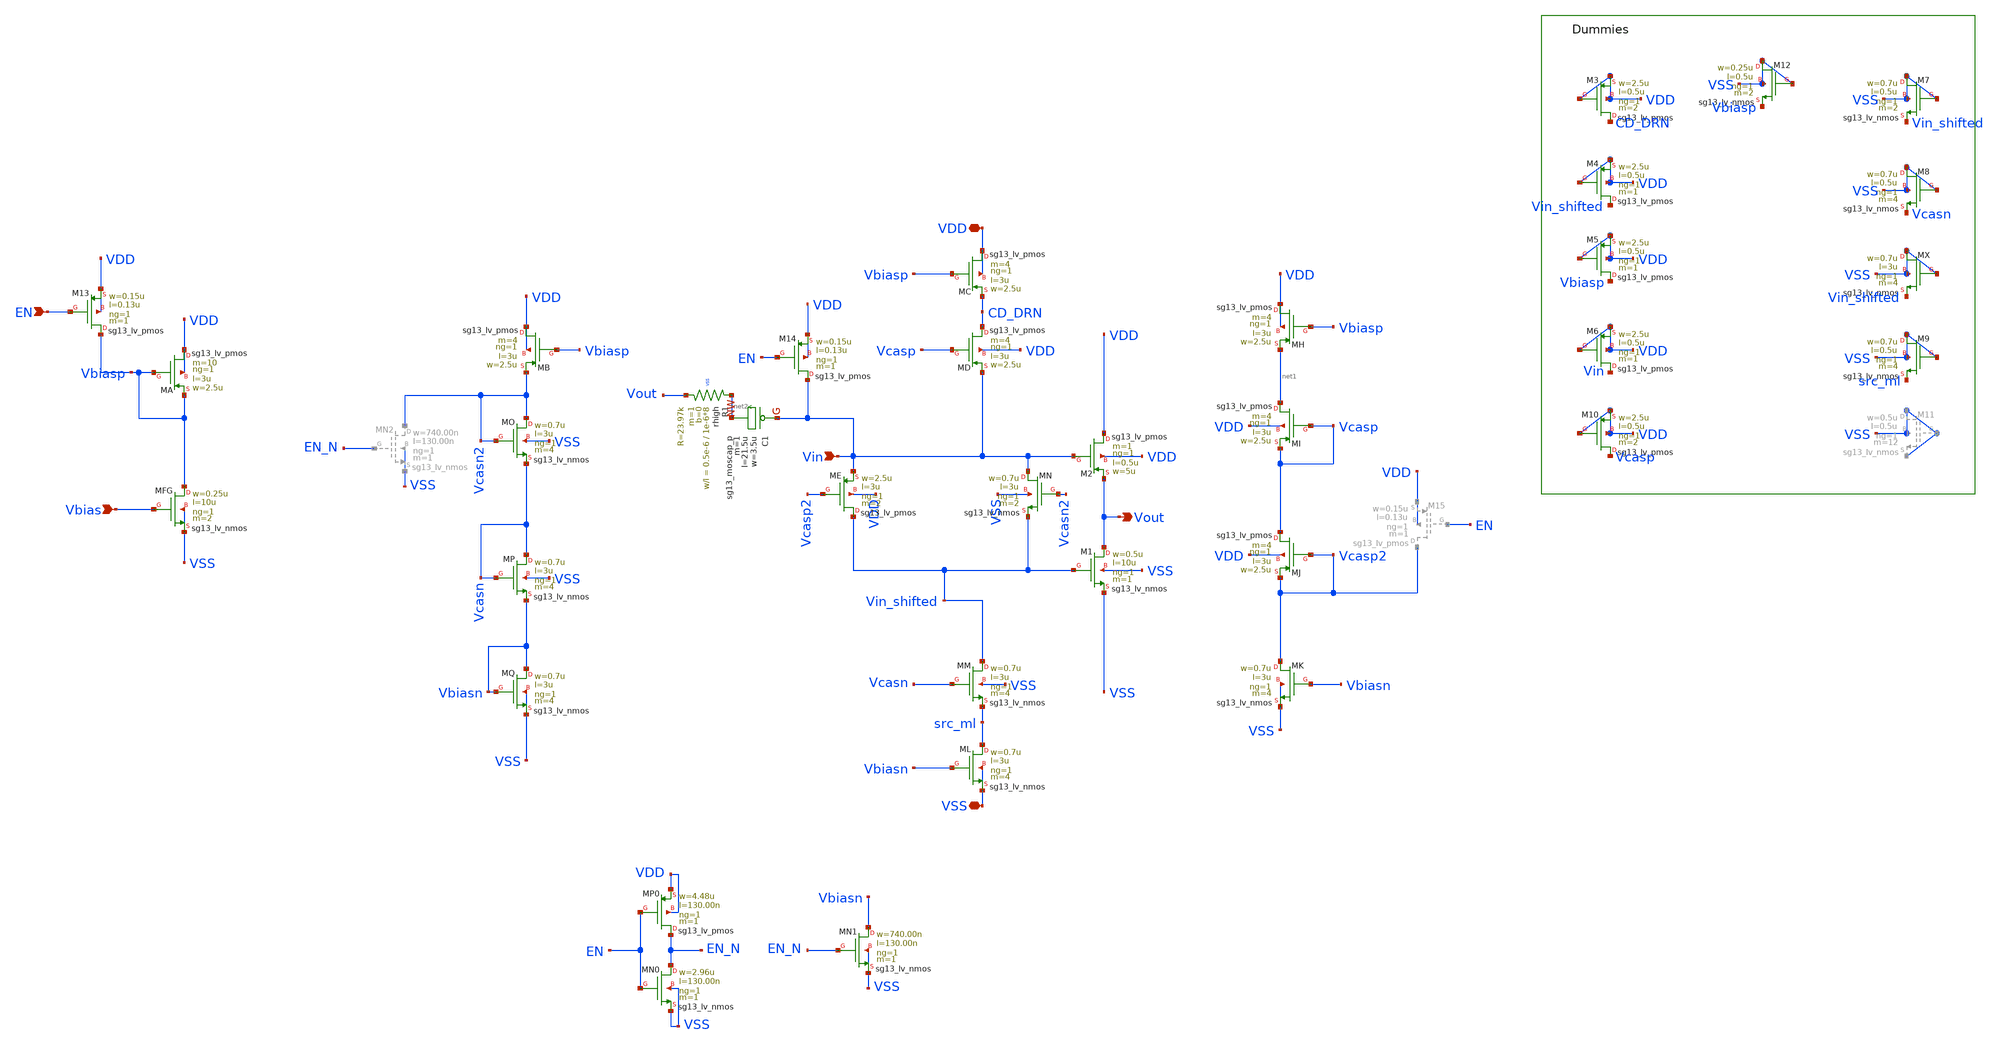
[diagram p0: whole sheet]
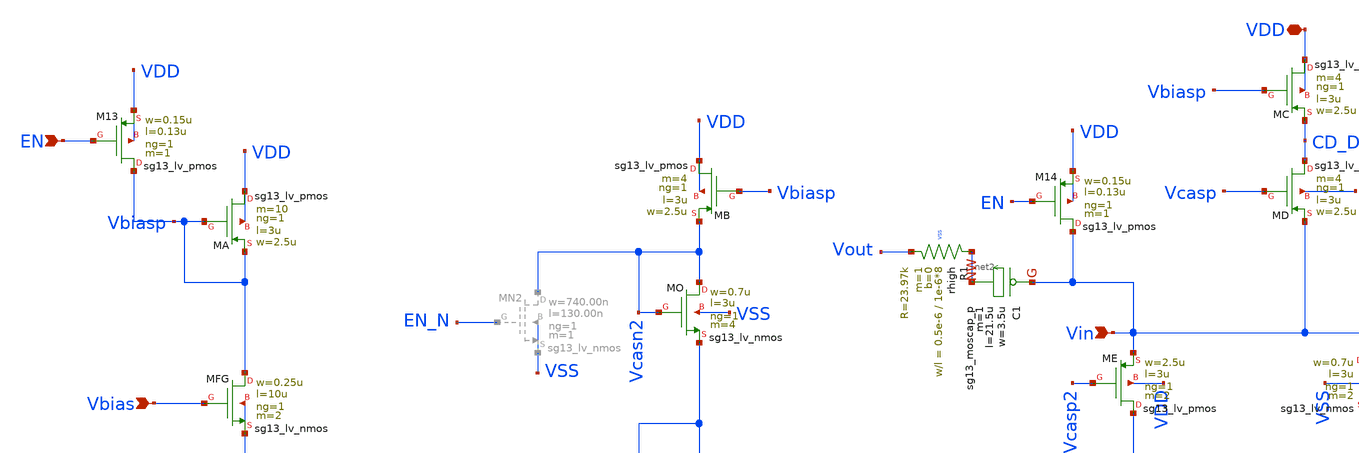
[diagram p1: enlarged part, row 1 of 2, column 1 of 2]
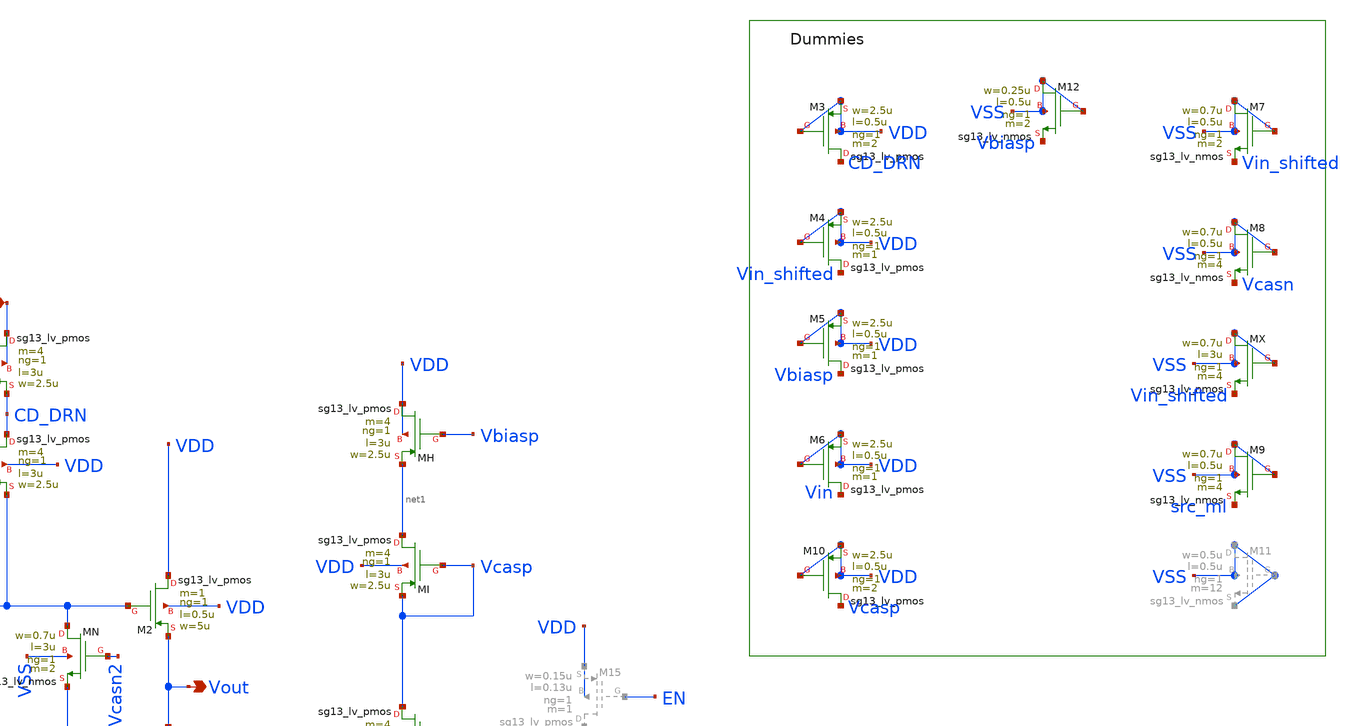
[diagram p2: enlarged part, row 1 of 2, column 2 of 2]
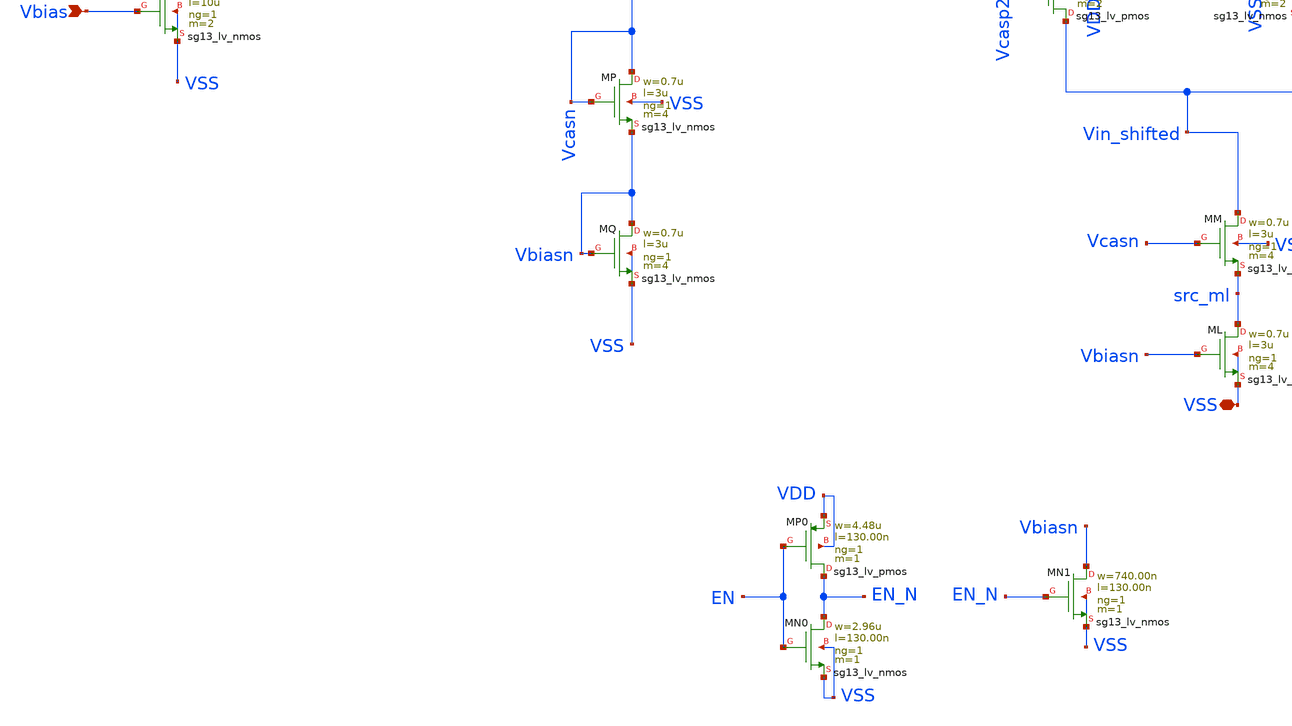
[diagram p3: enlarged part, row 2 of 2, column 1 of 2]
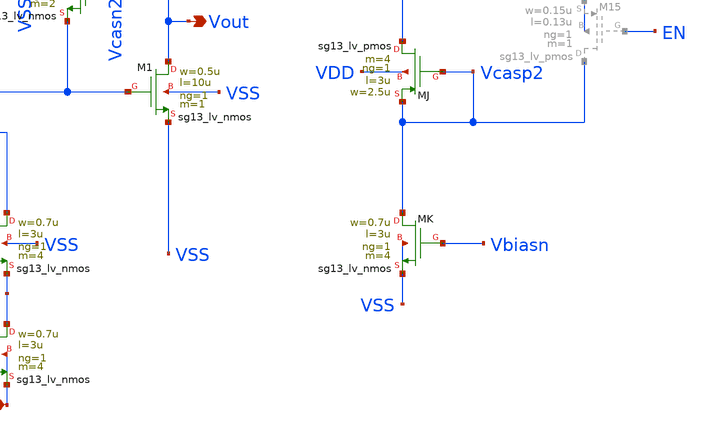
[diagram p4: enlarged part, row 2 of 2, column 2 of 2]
** sch_path: schema/ota_cmfb_core/ota_cmfb_core_push_pull_output_stage.sch
**.subckt ota_cmfb_core_push_pull_output_stage VSS VDD Vbias Vin Vout EN
*.iopin VSS
*.iopin VDD
*.ipin Vbias
*.ipin Vin
*.opin Vout
*.ipin EN
XM1 Vout Vin_shifted VSS VSS sg13_lv_nmos w=0.5u l=10u ng=1 m=1 mm_ok=1
XM2 VDD Vin Vout VDD sg13_lv_pmos w=5u l=0.5u ng=1 m=1 mm_ok=1
XMC VDD Vbiasp CD_DRN VDD sg13_lv_pmos w=2.5u l=3u ng=1 m=4 mm_ok=1
XME Vin_shifted Vcasp2 Vin VDD sg13_lv_pmos w=2.5u l=3u ng=1 m=2 mm_ok=1
XMD CD_DRN Vcasp Vin VDD sg13_lv_pmos w=2.5u l=3u ng=1 m=4 mm_ok=1
XMN Vin Vcasn2 Vin_shifted VSS sg13_lv_nmos w=0.7u l=3u ng=1 m=2 mm_ok=1
XMH VDD Vbiasp net1 VDD sg13_lv_pmos w=2.5u l=3u ng=1 m=4 mm_ok=1
XMI net1 Vcasp Vcasp VDD sg13_lv_pmos w=2.5u l=3u ng=1 m=4 mm_ok=1
XMJ Vcasp Vcasp2 Vcasp2 VDD sg13_lv_pmos w=2.5u l=3u ng=1 m=4 mm_ok=1
XMB VDD Vbiasp Vcasn2 VDD sg13_lv_pmos w=2.5u l=3u ng=1 m=4 mm_ok=1
XMO Vcasn2 Vcasn2 Vcasn VSS sg13_lv_nmos w=0.7u l=3u ng=1 m=4 mm_ok=1
XR1 net2 Vout VSS rhigh w=0.5e-6 l=1e-6*8 m=1 b=0 mm_ok=1
XC1 Vin net2 sg13_moscap_p w=3.5u l=21.5u m=1 mm_ok=1
XMFG Vbiasp Vbias VSS VSS sg13_lv_nmos w=0.25u l=10u ng=1 m=2 mm_ok=1
XMA VDD Vbiasp Vbiasp VDD sg13_lv_pmos w=2.5u l=3u ng=1 m=10 mm_ok=1
XMP Vcasn Vcasn Vbiasn VSS sg13_lv_nmos w=0.7u l=3u ng=1 m=4 mm_ok=1
XMQ Vbiasn Vbiasn VSS VSS sg13_lv_nmos w=0.7u l=3u ng=1 m=4 mm_ok=1
XMM Vin_shifted Vcasn src_ml VSS sg13_lv_nmos w=0.7u l=3u ng=1 m=4 mm_ok=1
XML src_ml Vbiasn VSS VSS sg13_lv_nmos w=0.7u l=3u ng=1 m=4 mm_ok=1
XMK Vcasp2 Vbiasn VSS VSS sg13_lv_nmos w=0.7u l=3u ng=1 m=4 mm_ok=1
XM3 CD_DRN VDD VDD VDD sg13_lv_pmos w=2.5u l=0.5u ng=1 m=2 mm_ok=1
XM4 Vin_shifted VDD VDD VDD sg13_lv_pmos w=2.5u l=0.5u ng=1 m=1 mm_ok=1
XM5 Vbiasp VDD VDD VDD sg13_lv_pmos w=2.5u l=0.5u ng=1 m=1 mm_ok=1
XM6 Vin VDD VDD VDD sg13_lv_pmos w=2.5u l=0.5u ng=1 m=1 mm_ok=1
XM7 VSS VSS Vin_shifted VSS sg13_lv_nmos w=0.7u l=0.5u ng=1 m=2 mm_ok=1
XM8 VSS VSS Vcasn VSS sg13_lv_nmos w=0.7u l=0.5u ng=1 m=4 mm_ok=1
XMX VSS VSS Vin_shifted VSS sg13_lv_nmos w=0.7u l=3u ng=1 m=4 mm_ok=1
XM9 VSS VSS src_ml VSS sg13_lv_nmos w=0.7u l=0.5u ng=1 m=4 mm_ok=1
XM10 Vcasp VDD VDD VDD sg13_lv_pmos w=2.5u l=0.5u ng=1 m=2 mm_ok=1
XM12 VSS VSS Vbiasp VSS sg13_lv_nmos w=0.25u l=0.5u ng=1 m=2 mm_ok=1
XM13 Vbiasp EN VDD VDD sg13_lv_pmos w=0.15u l=0.13u ng=1 m=1 mm_ok=1
XMN0 EN_N EN VSS VSS sg13_lv_nmos w=2.96u l=130.00n ng=1 m=1 mm_ok=1
XMP0 EN_N EN VDD VDD sg13_lv_pmos w=4.48u l=130.00n ng=1 m=1 mm_ok=1
XMN1 Vbiasn EN_N VSS VSS sg13_lv_nmos w=740.00n l=130.00n ng=1 m=1 mm_ok=1
XM14 Vin EN VDD VDD sg13_lv_pmos w=0.15u l=0.13u ng=1 m=1 mm_ok=1
**.ends
.end
